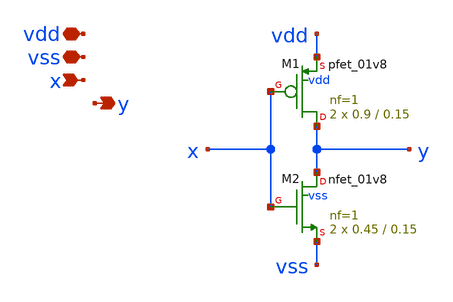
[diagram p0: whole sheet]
** sch_path: xschem/sc_not.sch
**.subckt sc_not vdd vss x y
*.iopin vdd
*.iopin vss
*.ipin x
*.opin y
XM1 y x vdd vdd sky130_fd_pr__pfet_01v8 L=0.15 W=0.9 nf=1 ad='int((1 + 1)/2) * 0.9 / 1 * 0.29' as='int((1 + 2)/2) * 0.9 / 1 * 0.29'
+ pd='2*int((1 + 1)/2) * (0.9 / 1 + 0.29)' ps='2*int((1 + 2)/2) * (0.9 / 1 + 0.29)' nrd='0.29 / 0.9 ' nrs='0.29 / 0.9 '
+ sa=0 sb=0 sd=0 mult=2 m=2
XM2 y x vss vss sky130_fd_pr__nfet_01v8 L=0.15 W=0.45 nf=1 ad='int((nf+1)/2) * W/nf * 0.29' as='int((nf+2)/2) * W/nf * 0.29'
+ pd='2*int((nf+1)/2) * (W/nf + 0.29)' ps='2*int((nf+2)/2) * (W/nf + 0.29)' nrd='0.29 / W' nrs='0.29 / W'
+ sa=0 sb=0 sd=0 mult=2 m=2
**.ends
.end
